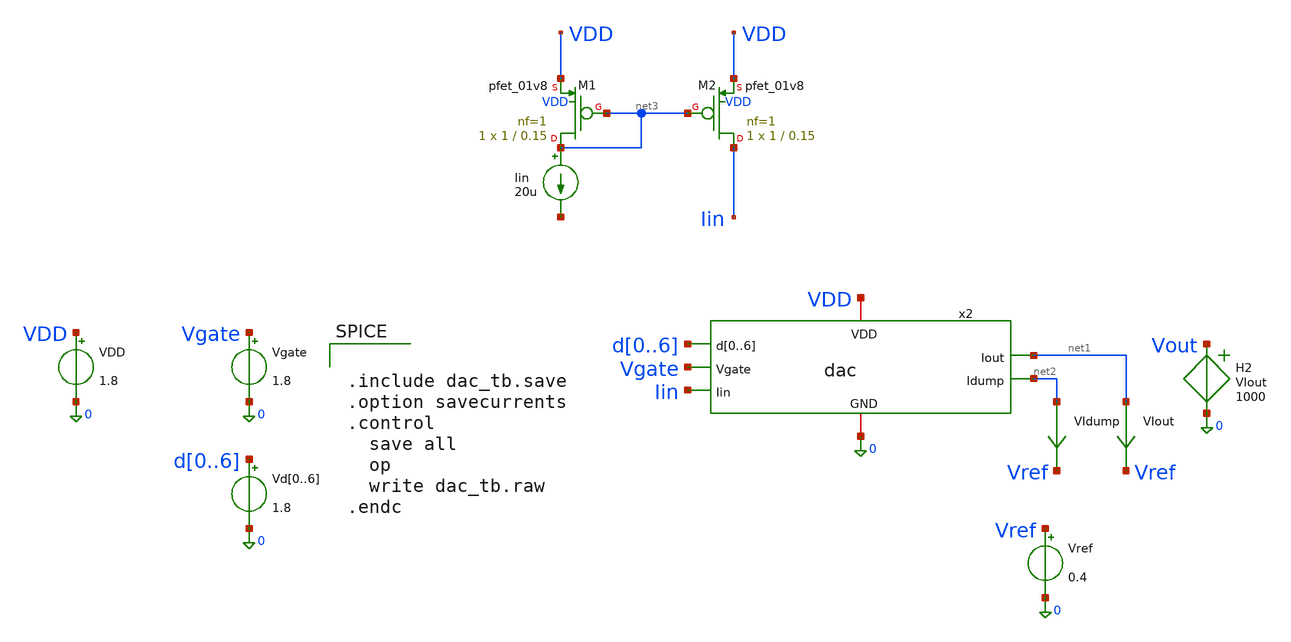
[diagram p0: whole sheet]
** sch_path: sch/archive/old/dac_tb.sch
**.subckt dac_tb
Iin net3 net4 20u
Vgate Vgate 0 1.8
.save i(vgate)
Vd0 d0 0 1.8
Vd1 d1 0 1.8
Vd2 d2 0 1.8
Vd3 d3 0 1.8
Vd4 d4 0 1.8
Vd5 d5 0 1.8
Vd6 d6 0 1.8
.save i(vd0)
.save i(vd1)
.save i(vd2)
.save i(vd3)
.save i(vd4)
.save i(vd5)
.save i(vd6)
VDD VDD 0 1.8
.save i(vdd)
H2 Vout 0 VIout 1000
VIout net1 Vref 0
.save i(viout)
VIdump net2 Vref 0
.save i(vidump)
XM1 net3 net3 VDD VDD sky130_fd_pr__pfet_01v8 L=0.15 W=1 nf=1 ad='int((1 + 1)/2) * 1 / 1 * 0.29' as='int((1 + 2)/2) * 1 / 1 * 0.29'
+ pd='2*int((1 + 1)/2) * (1 / 1 + 0.29)' ps='2*int((1 + 2)/2) * (1 / 1 + 0.29)' nrd='0.29 / 1 ' nrs='0.29 / 1 '
+ sa=0 sb=0 sd=0 mult=1 m=1
XM2 Iin net3 VDD VDD sky130_fd_pr__pfet_01v8 L=0.15 W=1 nf=1 ad='int((1 + 1)/2) * 1 / 1 * 0.29' as='int((1 + 2)/2) * 1 / 1 * 0.29'
+ pd='2*int((1 + 1)/2) * (1 / 1 + 0.29)' ps='2*int((1 + 2)/2) * (1 / 1 + 0.29)' nrd='0.29 / 1 ' nrs='0.29 / 1 '
+ sa=0 sb=0 sd=0 mult=1 m=1
Vref Vref 0 0.4
.save i(vref)
x2 VDD 0 d0 d1 d2 d3 d4 d5 d6 Vgate net1 net2 Iin dac
**** begin user architecture code

** opencircuitdesign pdks install
.lib $::SKYWATER_MODELS/sky130.lib.spice tt
.include $::SKYWATER_STDCELLS/sky130_fd_sc_hd.spice



.include dac_tb.save
.option savecurrents
.control
  save all
  op
  write dac_tb.raw
.endc




.control
  shell mkdir -p /foss/designs/sar_adc/sch/old/dac_sweep
  shell pwd
  set wr_vecnames
  set wr_singlescale
  unset appendwrite
  set code = 0
  while $code < 128
    let b0 = floor($code/64) % 2
    let b1 = floor($code/32) % 2
    let b2 = floor($code/16) % 2
    let b3 = floor($code/8) % 2
    let b4 = floor($code/4) % 2
    let b5 = floor($code/2) % 2
    let b6 = $code % 2

    let vh = 1.8
    let v0 = b0*vh
    let v1 = b1*vh
    let v2 = b2*vh
    let v3 = b3*vh
    let v4 = b4*vh
    let v5 = b5*vh
    let v6 = b6*vh

    alter Vd0 $&v0
    alter Vd1 $&v1
    alter Vd2 $&v2
    alter Vd3 $&v3
    alter Vd4 $&v4
    alter Vd5 $&v5
    alter Vd6 $&v6

    op
    let cv = $code
    wrdata /foss/designs/sar_adc/sch/old/dac_sweep/dac_tb.txt cv vout

    unset wr_vecnames
    set appendwrite
    let n = $code + 1
    set code = $&n
  end
.endc


**** end user architecture code
**.ends

* expanding   symbol:  /foss/designs/sar_adc/sch/old/dac.sym # of pins=7
** sym_path: sch/archive/old/dac.sym
** sch_path: sch/archive/old/dac.sch
.subckt dac VDD GND d0 d1 d2 d3 d4 d5 d6 Vgate Iout Idump Iin
*.ipin d0,d1,d2,d3,d4,d5,d6
*.opin Iout
*.iopin VDD
*.iopin GND
*.ipin Vgate
*.opin Idump
*.ipin Iin
XM7 Iin Vgate net1 GND sky130_fd_pr__nfet_01v8 L=3 W=1 nf=1 ad='int((1 + 1)/2) * 1 / 1 * 0.29' as='int((1 + 2)/2) * 1 / 1 * 0.29'
+ pd='2*int((1 + 1)/2) * (1 / 1 + 0.29)' ps='2*int((1 + 2)/2) * (1 / 1 + 0.29)' nrd='0.29 / 1 ' nrs='0.29 / 1 '
+ sa=0 sb=0 sd=0 mult=1 m=1
XM1 net1 d0 Iout GND sky130_fd_pr__nfet_01v8 L=3 W=1 nf=1 ad='int((1 + 1)/2) * 1 / 1 * 0.29' as='int((1 + 2)/2) * 1 / 1 * 0.29'
+ pd='2*int((1 + 1)/2) * (1 / 1 + 0.29)' ps='2*int((1 + 2)/2) * (1 / 1 + 0.29)' nrd='0.29 / 1 ' nrs='0.29 / 1 '
+ sa=0 sb=0 sd=0 mult=1 m=1
XM10 Iin Vgate net3 GND sky130_fd_pr__nfet_01v8 L=3 W=1 nf=1 ad='int((1 + 1)/2) * 1 / 1 * 0.29' as='int((1 + 2)/2) * 1 / 1 * 0.29'
+ pd='2*int((1 + 1)/2) * (1 / 1 + 0.29)' ps='2*int((1 + 2)/2) * (1 / 1 + 0.29)' nrd='0.29 / 1 ' nrs='0.29 / 1 '
+ sa=0 sb=0 sd=0 mult=1 m=1
x1 d0 GND GND VDD VDD net2 sky130_fd_sc_hd__inv_1
XM11 net1 net2 Idump GND sky130_fd_pr__nfet_01v8 L=3 W=1 nf=1 ad='int((1 + 1)/2) * 1 / 1 * 0.29' as='int((1 + 2)/2) * 1 / 1 * 0.29'
+ pd='2*int((1 + 1)/2) * (1 / 1 + 0.29)' ps='2*int((1 + 2)/2) * (1 / 1 + 0.29)' nrd='0.29 / 1 ' nrs='0.29 / 1 '
+ sa=0 sb=0 sd=0 mult=1 m=1
XM2 net3 Vgate net4 GND sky130_fd_pr__nfet_01v8 L=3 W=1 nf=1 ad='int((1 + 1)/2) * 1 / 1 * 0.29' as='int((1 + 2)/2) * 1 / 1 * 0.29'
+ pd='2*int((1 + 1)/2) * (1 / 1 + 0.29)' ps='2*int((1 + 2)/2) * (1 / 1 + 0.29)' nrd='0.29 / 1 ' nrs='0.29 / 1 '
+ sa=0 sb=0 sd=0 mult=1 m=1
XM3 net4 d1 Iout GND sky130_fd_pr__nfet_01v8 L=3 W=1 nf=1 ad='int((1 + 1)/2) * 1 / 1 * 0.29' as='int((1 + 2)/2) * 1 / 1 * 0.29'
+ pd='2*int((1 + 1)/2) * (1 / 1 + 0.29)' ps='2*int((1 + 2)/2) * (1 / 1 + 0.29)' nrd='0.29 / 1 ' nrs='0.29 / 1 '
+ sa=0 sb=0 sd=0 mult=1 m=1
XM4 net3 Vgate net6 GND sky130_fd_pr__nfet_01v8 L=3 W=1 nf=1 ad='int((1 + 1)/2) * 1 / 1 * 0.29' as='int((1 + 2)/2) * 1 / 1 * 0.29'
+ pd='2*int((1 + 1)/2) * (1 / 1 + 0.29)' ps='2*int((1 + 2)/2) * (1 / 1 + 0.29)' nrd='0.29 / 1 ' nrs='0.29 / 1 '
+ sa=0 sb=0 sd=0 mult=1 m=1
x2 d1 GND GND VDD VDD net5 sky130_fd_sc_hd__inv_1
XM5 net4 net5 Idump GND sky130_fd_pr__nfet_01v8 L=3 W=1 nf=1 ad='int((1 + 1)/2) * 1 / 1 * 0.29' as='int((1 + 2)/2) * 1 / 1 * 0.29'
+ pd='2*int((1 + 1)/2) * (1 / 1 + 0.29)' ps='2*int((1 + 2)/2) * (1 / 1 + 0.29)' nrd='0.29 / 1 ' nrs='0.29 / 1 '
+ sa=0 sb=0 sd=0 mult=1 m=1
XM6 net6 Vgate net7 GND sky130_fd_pr__nfet_01v8 L=3 W=1 nf=1 ad='int((1 + 1)/2) * 1 / 1 * 0.29' as='int((1 + 2)/2) * 1 / 1 * 0.29'
+ pd='2*int((1 + 1)/2) * (1 / 1 + 0.29)' ps='2*int((1 + 2)/2) * (1 / 1 + 0.29)' nrd='0.29 / 1 ' nrs='0.29 / 1 '
+ sa=0 sb=0 sd=0 mult=1 m=1
XM8 net7 d2 Iout GND sky130_fd_pr__nfet_01v8 L=3 W=1 nf=1 ad='int((1 + 1)/2) * 1 / 1 * 0.29' as='int((1 + 2)/2) * 1 / 1 * 0.29'
+ pd='2*int((1 + 1)/2) * (1 / 1 + 0.29)' ps='2*int((1 + 2)/2) * (1 / 1 + 0.29)' nrd='0.29 / 1 ' nrs='0.29 / 1 '
+ sa=0 sb=0 sd=0 mult=1 m=1
XM9 net6 Vgate net9 GND sky130_fd_pr__nfet_01v8 L=3 W=1 nf=1 ad='int((1 + 1)/2) * 1 / 1 * 0.29' as='int((1 + 2)/2) * 1 / 1 * 0.29'
+ pd='2*int((1 + 1)/2) * (1 / 1 + 0.29)' ps='2*int((1 + 2)/2) * (1 / 1 + 0.29)' nrd='0.29 / 1 ' nrs='0.29 / 1 '
+ sa=0 sb=0 sd=0 mult=1 m=1
x3 d2 GND GND VDD VDD net8 sky130_fd_sc_hd__inv_1
XM12 net7 net8 Idump GND sky130_fd_pr__nfet_01v8 L=3 W=1 nf=1 ad='int((1 + 1)/2) * 1 / 1 * 0.29' as='int((1 + 2)/2) * 1 / 1 * 0.29'
+ pd='2*int((1 + 1)/2) * (1 / 1 + 0.29)' ps='2*int((1 + 2)/2) * (1 / 1 + 0.29)' nrd='0.29 / 1 ' nrs='0.29 / 1 '
+ sa=0 sb=0 sd=0 mult=1 m=1
XM13 net9 Vgate net10 GND sky130_fd_pr__nfet_01v8 L=3 W=1 nf=1 ad='int((1 + 1)/2) * 1 / 1 * 0.29' as='int((1 + 2)/2) * 1 / 1 * 0.29'
+ pd='2*int((1 + 1)/2) * (1 / 1 + 0.29)' ps='2*int((1 + 2)/2) * (1 / 1 + 0.29)' nrd='0.29 / 1 ' nrs='0.29 / 1 '
+ sa=0 sb=0 sd=0 mult=1 m=1
XM14 net10 d3 Iout GND sky130_fd_pr__nfet_01v8 L=3 W=1 nf=1 ad='int((1 + 1)/2) * 1 / 1 * 0.29' as='int((1 + 2)/2) * 1 / 1 * 0.29'
+ pd='2*int((1 + 1)/2) * (1 / 1 + 0.29)' ps='2*int((1 + 2)/2) * (1 / 1 + 0.29)' nrd='0.29 / 1 ' nrs='0.29 / 1 '
+ sa=0 sb=0 sd=0 mult=1 m=1
XM15 net9 Vgate net12 GND sky130_fd_pr__nfet_01v8 L=3 W=1 nf=1 ad='int((1 + 1)/2) * 1 / 1 * 0.29' as='int((1 + 2)/2) * 1 / 1 * 0.29'
+ pd='2*int((1 + 1)/2) * (1 / 1 + 0.29)' ps='2*int((1 + 2)/2) * (1 / 1 + 0.29)' nrd='0.29 / 1 ' nrs='0.29 / 1 '
+ sa=0 sb=0 sd=0 mult=1 m=1
x4 d3 GND GND VDD VDD net11 sky130_fd_sc_hd__inv_1
XM16 net10 net11 Idump GND sky130_fd_pr__nfet_01v8 L=3 W=1 nf=1 ad='int((1 + 1)/2) * 1 / 1 * 0.29' as='int((1 + 2)/2) * 1 / 1 * 0.29'
+ pd='2*int((1 + 1)/2) * (1 / 1 + 0.29)' ps='2*int((1 + 2)/2) * (1 / 1 + 0.29)' nrd='0.29 / 1 ' nrs='0.29 / 1 '
+ sa=0 sb=0 sd=0 mult=1 m=1
XM17 net12 Vgate net13 GND sky130_fd_pr__nfet_01v8 L=3 W=1 nf=1 ad='int((1 + 1)/2) * 1 / 1 * 0.29' as='int((1 + 2)/2) * 1 / 1 * 0.29'
+ pd='2*int((1 + 1)/2) * (1 / 1 + 0.29)' ps='2*int((1 + 2)/2) * (1 / 1 + 0.29)' nrd='0.29 / 1 ' nrs='0.29 / 1 '
+ sa=0 sb=0 sd=0 mult=1 m=1
XM18 net13 d4 Iout GND sky130_fd_pr__nfet_01v8 L=3 W=1 nf=1 ad='int((1 + 1)/2) * 1 / 1 * 0.29' as='int((1 + 2)/2) * 1 / 1 * 0.29'
+ pd='2*int((1 + 1)/2) * (1 / 1 + 0.29)' ps='2*int((1 + 2)/2) * (1 / 1 + 0.29)' nrd='0.29 / 1 ' nrs='0.29 / 1 '
+ sa=0 sb=0 sd=0 mult=1 m=1
XM19 net12 Vgate net15 GND sky130_fd_pr__nfet_01v8 L=3 W=1 nf=1 ad='int((1 + 1)/2) * 1 / 1 * 0.29' as='int((1 + 2)/2) * 1 / 1 * 0.29'
+ pd='2*int((1 + 1)/2) * (1 / 1 + 0.29)' ps='2*int((1 + 2)/2) * (1 / 1 + 0.29)' nrd='0.29 / 1 ' nrs='0.29 / 1 '
+ sa=0 sb=0 sd=0 mult=1 m=1
x5 d4 GND GND VDD VDD net14 sky130_fd_sc_hd__inv_1
XM20 net13 net14 Idump GND sky130_fd_pr__nfet_01v8 L=3 W=1 nf=1 ad='int((1 + 1)/2) * 1 / 1 * 0.29' as='int((1 + 2)/2) * 1 / 1 * 0.29'
+ pd='2*int((1 + 1)/2) * (1 / 1 + 0.29)' ps='2*int((1 + 2)/2) * (1 / 1 + 0.29)' nrd='0.29 / 1 ' nrs='0.29 / 1 '
+ sa=0 sb=0 sd=0 mult=1 m=1
XM21 net15 Vgate net16 GND sky130_fd_pr__nfet_01v8 L=3 W=1 nf=1 ad='int((1 + 1)/2) * 1 / 1 * 0.29' as='int((1 + 2)/2) * 1 / 1 * 0.29'
+ pd='2*int((1 + 1)/2) * (1 / 1 + 0.29)' ps='2*int((1 + 2)/2) * (1 / 1 + 0.29)' nrd='0.29 / 1 ' nrs='0.29 / 1 '
+ sa=0 sb=0 sd=0 mult=1 m=1
XM22 net16 d5 Iout GND sky130_fd_pr__nfet_01v8 L=3 W=1 nf=1 ad='int((1 + 1)/2) * 1 / 1 * 0.29' as='int((1 + 2)/2) * 1 / 1 * 0.29'
+ pd='2*int((1 + 1)/2) * (1 / 1 + 0.29)' ps='2*int((1 + 2)/2) * (1 / 1 + 0.29)' nrd='0.29 / 1 ' nrs='0.29 / 1 '
+ sa=0 sb=0 sd=0 mult=1 m=1
XM23 net15 Vgate net18 GND sky130_fd_pr__nfet_01v8 L=3 W=1 nf=1 ad='int((1 + 1)/2) * 1 / 1 * 0.29' as='int((1 + 2)/2) * 1 / 1 * 0.29'
+ pd='2*int((1 + 1)/2) * (1 / 1 + 0.29)' ps='2*int((1 + 2)/2) * (1 / 1 + 0.29)' nrd='0.29 / 1 ' nrs='0.29 / 1 '
+ sa=0 sb=0 sd=0 mult=1 m=1
x6 d5 GND GND VDD VDD net17 sky130_fd_sc_hd__inv_1
XM24 net16 net17 Idump GND sky130_fd_pr__nfet_01v8 L=3 W=1 nf=1 ad='int((1 + 1)/2) * 1 / 1 * 0.29' as='int((1 + 2)/2) * 1 / 1 * 0.29'
+ pd='2*int((1 + 1)/2) * (1 / 1 + 0.29)' ps='2*int((1 + 2)/2) * (1 / 1 + 0.29)' nrd='0.29 / 1 ' nrs='0.29 / 1 '
+ sa=0 sb=0 sd=0 mult=1 m=1
XM25 net18 Vgate net19 GND sky130_fd_pr__nfet_01v8 L=3 W=1 nf=1 ad='int((1 + 1)/2) * 1 / 1 * 0.29' as='int((1 + 2)/2) * 1 / 1 * 0.29'
+ pd='2*int((1 + 1)/2) * (1 / 1 + 0.29)' ps='2*int((1 + 2)/2) * (1 / 1 + 0.29)' nrd='0.29 / 1 ' nrs='0.29 / 1 '
+ sa=0 sb=0 sd=0 mult=1 m=1
XM26 net19 d6 Iout GND sky130_fd_pr__nfet_01v8 L=3 W=1 nf=1 ad='int((1 + 1)/2) * 1 / 1 * 0.29' as='int((1 + 2)/2) * 1 / 1 * 0.29'
+ pd='2*int((1 + 1)/2) * (1 / 1 + 0.29)' ps='2*int((1 + 2)/2) * (1 / 1 + 0.29)' nrd='0.29 / 1 ' nrs='0.29 / 1 '
+ sa=0 sb=0 sd=0 mult=1 m=1
XM27 net18 Vgate net21 GND sky130_fd_pr__nfet_01v8 L=3 W=1 nf=1 ad='int((1 + 1)/2) * 1 / 1 * 0.29' as='int((1 + 2)/2) * 1 / 1 * 0.29'
+ pd='2*int((1 + 1)/2) * (1 / 1 + 0.29)' ps='2*int((1 + 2)/2) * (1 / 1 + 0.29)' nrd='0.29 / 1 ' nrs='0.29 / 1 '
+ sa=0 sb=0 sd=0 mult=1 m=1
x7 d6 GND GND VDD VDD net20 sky130_fd_sc_hd__inv_1
XM28 net19 net20 Idump GND sky130_fd_pr__nfet_01v8 L=3 W=1 nf=1 ad='int((1 + 1)/2) * 1 / 1 * 0.29' as='int((1 + 2)/2) * 1 / 1 * 0.29'
+ pd='2*int((1 + 1)/2) * (1 / 1 + 0.29)' ps='2*int((1 + 2)/2) * (1 / 1 + 0.29)' nrd='0.29 / 1 ' nrs='0.29 / 1 '
+ sa=0 sb=0 sd=0 mult=1 m=1
XM29 net21 Vgate Idump GND sky130_fd_pr__nfet_01v8 L=3 W=1 nf=1 ad='int((1 + 1)/2) * 1 / 1 * 0.29' as='int((1 + 2)/2) * 1 / 1 * 0.29'
+ pd='2*int((1 + 1)/2) * (1 / 1 + 0.29)' ps='2*int((1 + 2)/2) * (1 / 1 + 0.29)' nrd='0.29 / 1 ' nrs='0.29 / 1 '
+ sa=0 sb=0 sd=0 mult=1 m=1
.ends

.end
